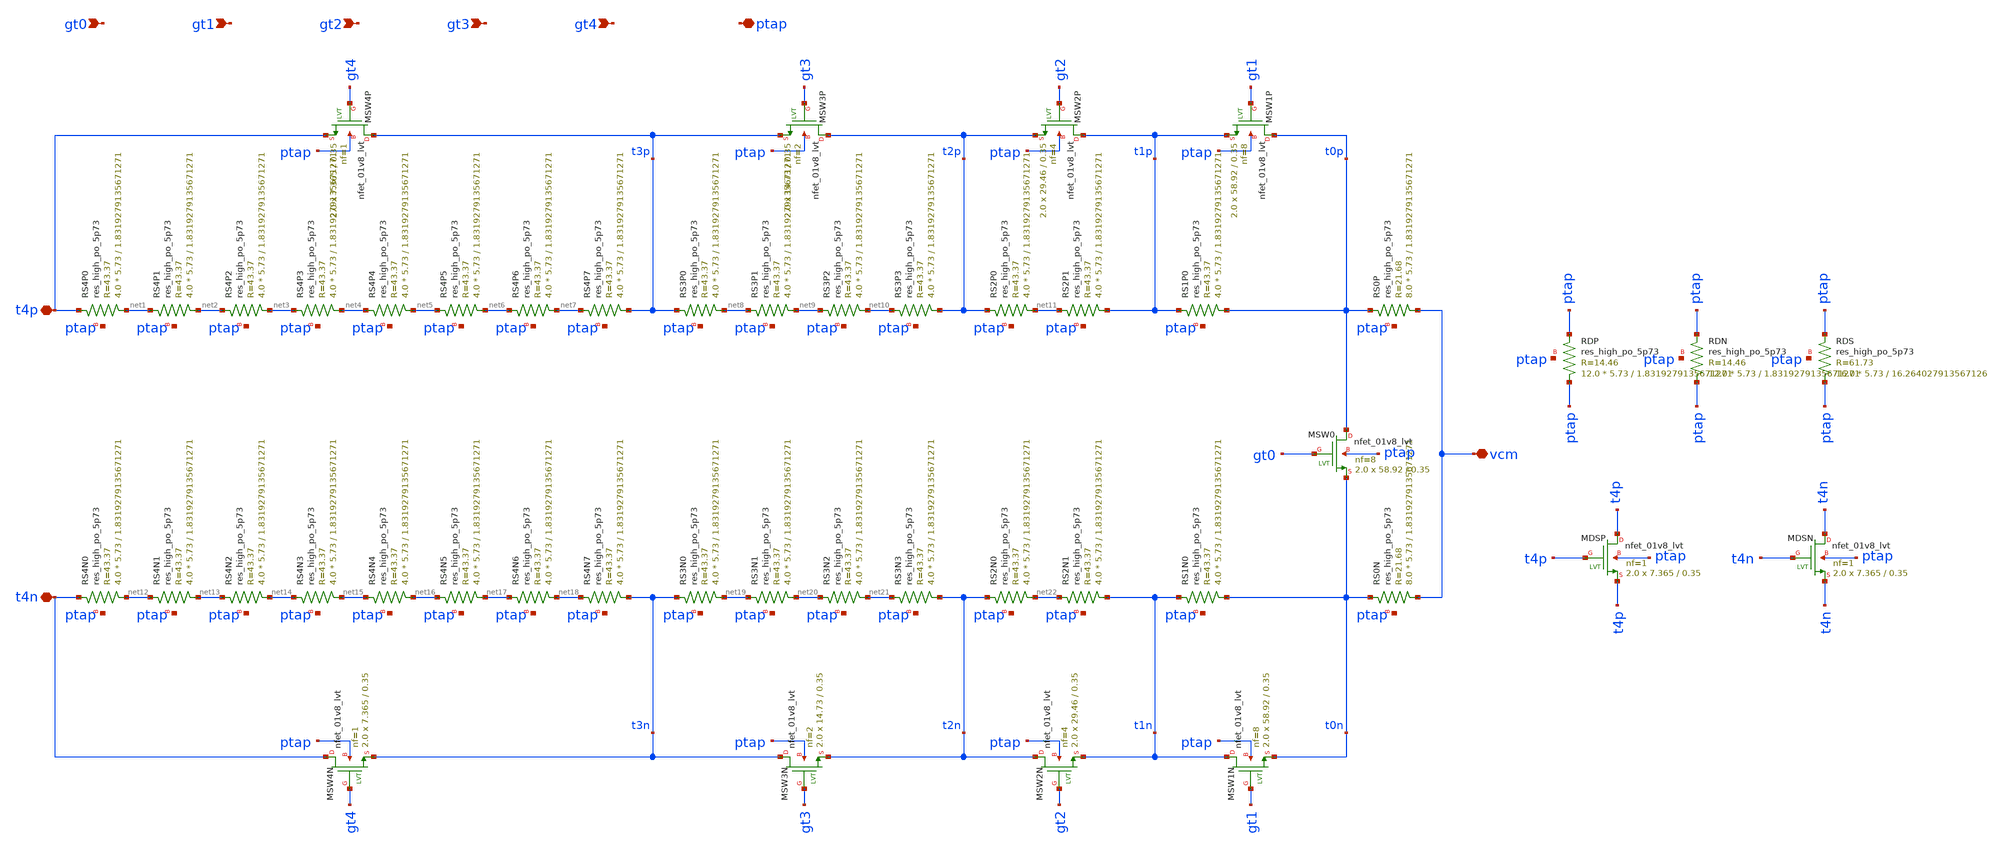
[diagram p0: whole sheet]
** sch_path: verification/porting/sky_replica_schematic/schematic/gain_trim.sch
**.subckt gain_trim t4p t4n vcm gt0 gt1 gt2 gt3 gt4 ptap
*.iopin t4p
*.iopin t4n
*.iopin vcm
*.ipin gt0
*.ipin gt1
*.ipin gt2
*.ipin gt3
*.ipin gt4
*.iopin ptap
XRS4P0 net1 t4p ptap sky130_fd_pr__res_high_po_5p73 L=1.8319279135671271 mult=4.0 m=4.0
XRS4P1 net2 net1 ptap sky130_fd_pr__res_high_po_5p73 L=1.8319279135671271 mult=4.0 m=4.0
XRS4P2 net3 net2 ptap sky130_fd_pr__res_high_po_5p73 L=1.8319279135671271 mult=4.0 m=4.0
XRS4P3 net4 net3 ptap sky130_fd_pr__res_high_po_5p73 L=1.8319279135671271 mult=4.0 m=4.0
XRS4P4 net5 net4 ptap sky130_fd_pr__res_high_po_5p73 L=1.8319279135671271 mult=4.0 m=4.0
XRS4P5 net6 net5 ptap sky130_fd_pr__res_high_po_5p73 L=1.8319279135671271 mult=4.0 m=4.0
XRS4P6 net7 net6 ptap sky130_fd_pr__res_high_po_5p73 L=1.8319279135671271 mult=4.0 m=4.0
XRS4P7 t3p net7 ptap sky130_fd_pr__res_high_po_5p73 L=1.8319279135671271 mult=4.0 m=4.0
XRS3P0 net8 t3p ptap sky130_fd_pr__res_high_po_5p73 L=1.8319279135671271 mult=4.0 m=4.0
XRS3P1 net9 net8 ptap sky130_fd_pr__res_high_po_5p73 L=1.8319279135671271 mult=4.0 m=4.0
XRS3P2 net10 net9 ptap sky130_fd_pr__res_high_po_5p73 L=1.8319279135671271 mult=4.0 m=4.0
XRS3P3 t2p net10 ptap sky130_fd_pr__res_high_po_5p73 L=1.8319279135671271 mult=4.0 m=4.0
XRS2P0 net11 t2p ptap sky130_fd_pr__res_high_po_5p73 L=1.8319279135671271 mult=4.0 m=4.0
XRS2P1 t1p net11 ptap sky130_fd_pr__res_high_po_5p73 L=1.8319279135671271 mult=4.0 m=4.0
XRS1P0 t0p t1p ptap sky130_fd_pr__res_high_po_5p73 L=1.8319279135671271 mult=4.0 m=4.0
XRS0P vcm t0p ptap sky130_fd_pr__res_high_po_5p73 L=1.8319279135671271 mult=8.0 m=8.0
XMSW4P t3p gt4 t4p ptap sky130_fd_pr__nfet_01v8_lvt L=0.35 W=7.365 nf=1 ad=2.13585 as=2.13585
+ pd=15.31 ps=15.31 nrd=0.039375424304141204 nrs=0.039375424304141204 sa=0 sb=0 sd=0 mult=2.0 m=2.0
XMSW3P t2p gt3 t3p ptap sky130_fd_pr__nfet_01v8_lvt L=0.35 W=14.73 nf=2 ad=2.13585 as=4.2717
+ pd=15.31 ps=30.62 nrd=0.019687712152070602 nrs=0.019687712152070602 sa=0 sb=0 sd=0 mult=2.0 m=2.0
XMSW2P t1p gt2 t2p ptap sky130_fd_pr__nfet_01v8_lvt L=0.35 W=29.46 nf=4 ad=4.2717 as=6.40755
+ pd=30.62 ps=45.93 nrd=0.009843856076035301 nrs=0.009843856076035301 sa=0 sb=0 sd=0 mult=2.0 m=2.0
XMSW1P t0p gt1 t1p ptap sky130_fd_pr__nfet_01v8_lvt L=0.35 W=58.92 nf=8 ad=8.5434 as=10.67925
+ pd=61.24 ps=76.55 nrd=0.0049219280380176506 nrs=0.0049219280380176506 sa=0 sb=0 sd=0 mult=2.0 m=2.0
XRS4N0 net12 t4n ptap sky130_fd_pr__res_high_po_5p73 L=1.8319279135671271 mult=4.0 m=4.0
XRS4N1 net13 net12 ptap sky130_fd_pr__res_high_po_5p73 L=1.8319279135671271 mult=4.0 m=4.0
XRS4N2 net14 net13 ptap sky130_fd_pr__res_high_po_5p73 L=1.8319279135671271 mult=4.0 m=4.0
XRS4N3 net15 net14 ptap sky130_fd_pr__res_high_po_5p73 L=1.8319279135671271 mult=4.0 m=4.0
XRS4N4 net16 net15 ptap sky130_fd_pr__res_high_po_5p73 L=1.8319279135671271 mult=4.0 m=4.0
XRS4N5 net17 net16 ptap sky130_fd_pr__res_high_po_5p73 L=1.8319279135671271 mult=4.0 m=4.0
XRS4N6 net18 net17 ptap sky130_fd_pr__res_high_po_5p73 L=1.8319279135671271 mult=4.0 m=4.0
XRS4N7 t3n net18 ptap sky130_fd_pr__res_high_po_5p73 L=1.8319279135671271 mult=4.0 m=4.0
XRS3N0 net19 t3n ptap sky130_fd_pr__res_high_po_5p73 L=1.8319279135671271 mult=4.0 m=4.0
XRS3N1 net20 net19 ptap sky130_fd_pr__res_high_po_5p73 L=1.8319279135671271 mult=4.0 m=4.0
XRS3N2 net21 net20 ptap sky130_fd_pr__res_high_po_5p73 L=1.8319279135671271 mult=4.0 m=4.0
XRS3N3 t2n net21 ptap sky130_fd_pr__res_high_po_5p73 L=1.8319279135671271 mult=4.0 m=4.0
XRS2N0 net22 t2n ptap sky130_fd_pr__res_high_po_5p73 L=1.8319279135671271 mult=4.0 m=4.0
XRS2N1 t1n net22 ptap sky130_fd_pr__res_high_po_5p73 L=1.8319279135671271 mult=4.0 m=4.0
XRS1N0 t0n t1n ptap sky130_fd_pr__res_high_po_5p73 L=1.8319279135671271 mult=4.0 m=4.0
XRS0N vcm t0n ptap sky130_fd_pr__res_high_po_5p73 L=1.8319279135671271 mult=8.0 m=8.0
XMSW4N t4n gt4 t3n ptap sky130_fd_pr__nfet_01v8_lvt L=0.35 W=7.365 nf=1 ad=2.13585 as=2.13585
+ pd=15.31 ps=15.31 nrd=0.039375424304141204 nrs=0.039375424304141204 sa=0 sb=0 sd=0 mult=2.0 m=2.0
XMSW3N t3n gt3 t2n ptap sky130_fd_pr__nfet_01v8_lvt L=0.35 W=14.73 nf=2 ad=2.13585 as=4.2717
+ pd=15.31 ps=30.62 nrd=0.019687712152070602 nrs=0.019687712152070602 sa=0 sb=0 sd=0 mult=2.0 m=2.0
XMSW2N t2n gt2 t1n ptap sky130_fd_pr__nfet_01v8_lvt L=0.35 W=29.46 nf=4 ad=4.2717 as=6.40755
+ pd=30.62 ps=45.93 nrd=0.009843856076035301 nrs=0.009843856076035301 sa=0 sb=0 sd=0 mult=2.0 m=2.0
XMSW1N t1n gt1 t0n ptap sky130_fd_pr__nfet_01v8_lvt L=0.35 W=58.92 nf=8 ad=8.5434 as=10.67925
+ pd=61.24 ps=76.55 nrd=0.0049219280380176506 nrs=0.0049219280380176506 sa=0 sb=0 sd=0 mult=2.0 m=2.0
XMSW0 t0p gt0 t0n ptap sky130_fd_pr__nfet_01v8_lvt L=0.35 W=58.92 nf=8 ad=8.5434 as=10.67925
+ pd=61.24 ps=76.55 nrd=0.0049219280380176506 nrs=0.0049219280380176506 sa=0 sb=0 sd=0 mult=2.0 m=2.0
XRDP ptap ptap ptap sky130_fd_pr__res_high_po_5p73 L=1.8319279135671271 mult=12.0 m=12.0
XRDN ptap ptap ptap sky130_fd_pr__res_high_po_5p73 L=1.8319279135671271 mult=12.0 m=12.0
XRDS ptap ptap ptap sky130_fd_pr__res_high_po_5p73 L=16.264027913567126 mult=16.0 m=16.0
XMDSP t4p t4p t4p ptap sky130_fd_pr__nfet_01v8_lvt L=0.35 W=7.365 nf=1 ad=2.13585 as=2.13585
+ pd=15.31 ps=15.31 nrd=0.039375424304141204 nrs=0.039375424304141204 sa=0 sb=0 sd=0 mult=2.0 m=2.0
XMDSN t4n t4n t4n ptap sky130_fd_pr__nfet_01v8_lvt L=0.35 W=7.365 nf=1 ad=2.13585 as=2.13585
+ pd=15.31 ps=15.31 nrd=0.039375424304141204 nrs=0.039375424304141204 sa=0 sb=0 sd=0 mult=2.0 m=2.0
**.ends
.end
